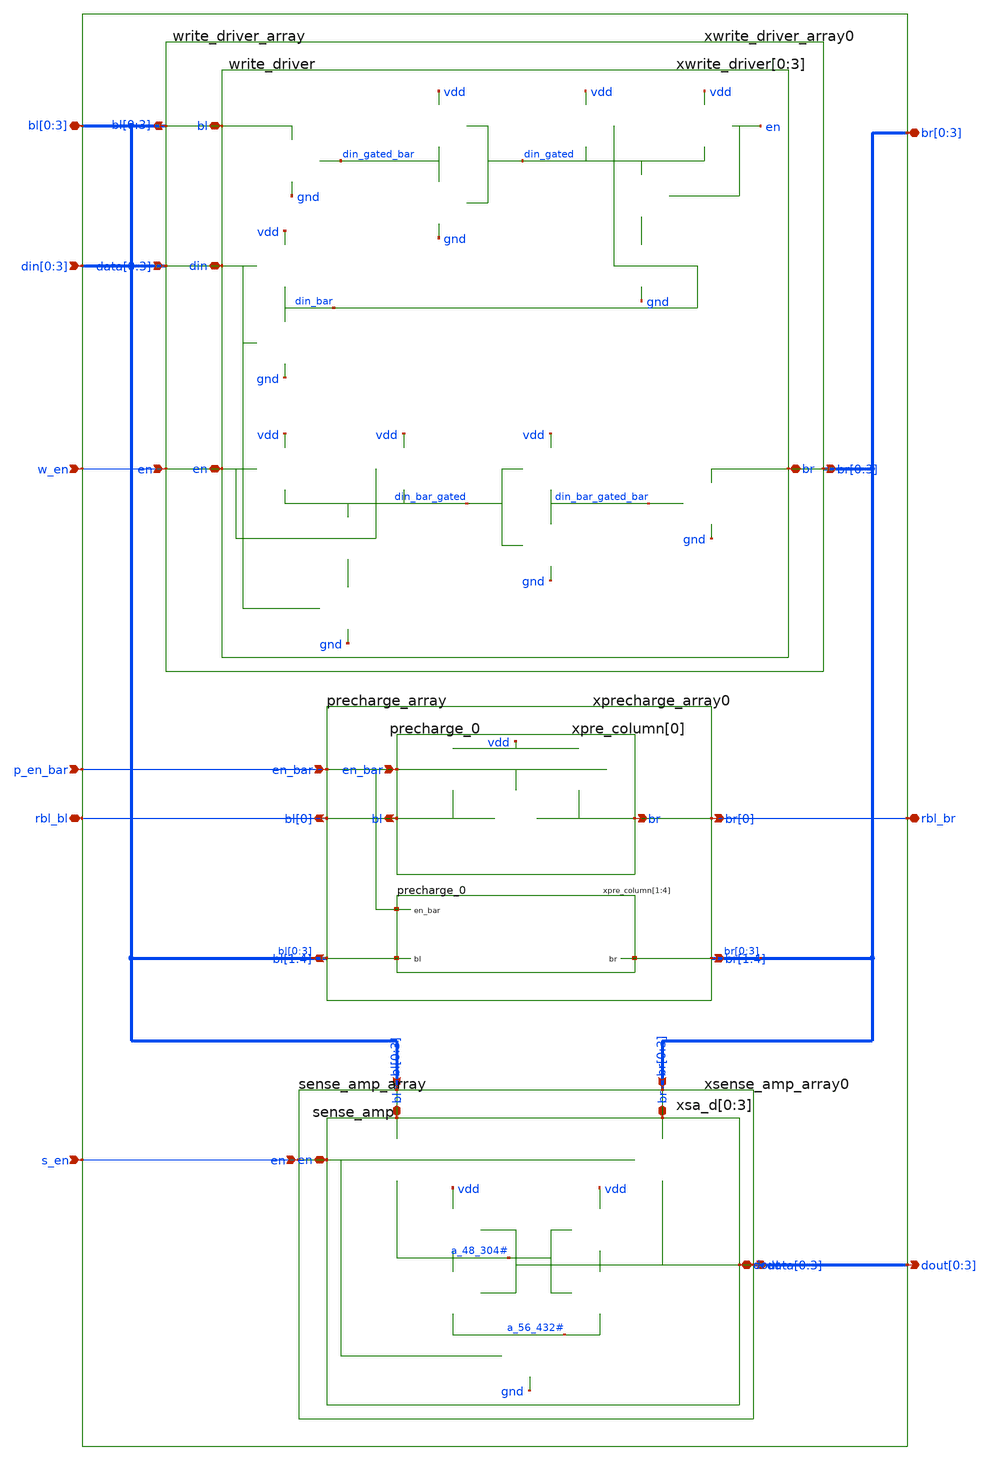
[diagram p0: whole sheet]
** sch_path: sram_4_16_scn4m/port_data.sch
**.subckt port_data rbl_bl rbl_br bl[0],bl[1],bl[2],bl[3] br[0],br[1],br[2],br[3]
*+ dout[0],dout[1],dout[2],dout[3] din[0],din[1],din[2],din[3] s_en p_en_bar w_en
*.iopin rbl_bl
*.iopin rbl_br
*.iopin bl[0],bl[1],bl[2],bl[3]
*.iopin br[0],br[1],br[2],br[3]
*.opin dout[0],dout[1],dout[2],dout[3]
*.ipin din[0],din[1],din[2],din[3]
*.ipin s_en
*.ipin p_en_bar
*.ipin w_en
xprecharge_array0 p_en_bar vdd precharge_array
xwrite_driver_array0 din[0] din[1] din[2] din[3] bl[0] bl[1] bl[2] bl[3] br[0] br[1] br[2] br[3]
+ w_en vdd gnd write_driver_array
xsense_amp_array0 dout[0] dout[1] dout[2] dout[3] bl[0] bl[1] bl[2] bl[3] br[0] br[1] br[2] br[3]
+ s_en vdd gnd sense_amp_array
**.ends

* expanding   symbol:  precharge_array.sch # of pins=5
** sym_path: sram_4_16_scn4m/precharge_array.sch
** sch_path: sram_4_16_scn4m/precharge_array.sch
.subckt precharge_array en_bar vdd
*.opin bl[0]
*.opin br[0]
*.ipin en_bar
*.opin bl[1],bl[2],bl[3],bl[4]
*.opin br[1],br[2],br[3],br[4]
xpre_column[0] bl[0] br[0] en_bar vdd precharge_0
xpre_column[1] bl[1] br[1] en_bar vdd precharge_0
xpre_column[2] bl[2] br[2] en_bar vdd precharge_0
xpre_column[3] bl[3] br[3] en_bar vdd precharge_0
xpre_column[4] bl[4] br[4] en_bar vdd precharge_0
.ends


* expanding   symbol:  write_driver_array.sch # of pins=4
** sym_path: sram_4_16_scn4m/write_driver_array.sch
** sch_path: sram_4_16_scn4m/write_driver_array.sch
.subckt write_driver_array data[0] data[1] data[2] data[3] bl[0] bl[1] bl[2] bl[3] br[0] br[1] br[2]
+ br[3] en vdd gnd
*.ipin data[0],data[1],data[2],data[3]
*.opin bl[0],bl[1],bl[2],bl[3]
*.opin br[0],br[1],br[2],br[3]
*.ipin en
xwrite_driver[0] data[0] bl[0] br[0] en vdd gnd write_driver
xwrite_driver[1] data[1] bl[1] br[1] en vdd gnd write_driver
xwrite_driver[2] data[2] bl[2] br[2] en vdd gnd write_driver
xwrite_driver[3] data[3] bl[3] br[3] en vdd gnd write_driver
.ends


* expanding   symbol:  sense_amp_array.sch # of pins=4
** sym_path: sram_4_16_scn4m/sense_amp_array.sch
** sch_path: sram_4_16_scn4m/sense_amp_array.sch
.subckt sense_amp_array data[0] data[1] data[2] data[3] bl[0] bl[1] bl[2] bl[3] br[0] br[1] br[2]
+ br[3] en vdd gnd
*.opin data[0],data[1],data[2],data[3]
*.ipin bl[0],bl[1],bl[2],bl[3]
*.ipin br[0],br[1],br[2],br[3]
*.ipin en
xsa_d[0] bl[0] br[0] data[0] en vdd gnd sense_amp
xsa_d[1] bl[1] br[1] data[1] en vdd gnd sense_amp
xsa_d[2] bl[2] br[2] data[2] en vdd gnd sense_amp
xsa_d[3] bl[3] br[3] data[3] en vdd gnd sense_amp
.ends


* expanding   symbol:  precharge_0.sch # of pins=3
** sym_path: sram_4_16_scn4m/precharge_0.sch
** sch_path: sram_4_16_scn4m/precharge_0.sch
.subckt precharge_0 bl br en_bar vdd
*.opin bl
*.opin br
*.ipin en_bar
XMupper_pmos1 bl en_bar vdd vdd sky130_fd_pr__pfet_01v8 L=0.4 W=1.6 nf=1 ad='int((nf+1)/2) * W/nf * 0.29'
+ as='int((nf+2)/2) * W/nf * 0.29' pd='2*int((nf+1)/2) * (W/nf + 0.29)' ps='2*int((nf+2)/2) * (W/nf + 0.29)'
+ nrd='0.29 / W' nrs='0.29 / W' sa=0 sb=0 sd=0 mult=1 m=1
XMupper_pmos2 br en_bar vdd vdd sky130_fd_pr__pfet_01v8 L=0.4 W=1.6 nf=1 ad='int((nf+1)/2) * W/nf * 0.29'
+ as='int((nf+2)/2) * W/nf * 0.29' pd='2*int((nf+1)/2) * (W/nf + 0.29)' ps='2*int((nf+2)/2) * (W/nf + 0.29)'
+ nrd='0.29 / W' nrs='0.29 / W' sa=0 sb=0 sd=0 mult=1 m=1
XMlower_pmos br en_bar bl vdd sky130_fd_pr__pfet_01v8 L=0.4 W=1.6 nf=1 ad='int((nf+1)/2) * W/nf * 0.29'
+ as='int((nf+2)/2) * W/nf * 0.29' pd='2*int((nf+1)/2) * (W/nf + 0.29)' ps='2*int((nf+2)/2) * (W/nf + 0.29)'
+ nrd='0.29 / W' nrs='0.29 / W' sa=0 sb=0 sd=0 mult=1 m=1
.ends


* expanding   symbol:  write_driver.sch # of pins=4
** sym_path: sram_4_16_scn4m/write_driver.sch
** sch_path: sram_4_16_scn4m/write_driver.sch
.subckt write_driver din bl br en vdd gnd
*.iopin din
*.iopin bl
*.iopin br
*.iopin en
XM_1 din_bar din gnd gnd sky130_fd_pr__nfet_01v8 L=0.4 W=1.4 nf=1 ad='int((nf+1)/2) * W/nf * 0.29' as='int((nf+2)/2) * W/nf * 0.29'
+ pd='2*int((nf+1)/2) * (W/nf + 0.29)' ps='2*int((nf+2)/2) * (W/nf + 0.29)' nrd='0.29 / W' nrs='0.29 / W'
+ sa=0 sb=0 sd=0 mult=1 m=1
XM_2 din_bar din vdd vdd sky130_fd_pr__pfet_01v8 L=0.4 W=1.4 nf=1 ad='int((nf+1)/2) * W/nf * 0.29' as='int((nf+2)/2) * W/nf * 0.29'
+ pd='2*int((nf+1)/2) * (W/nf + 0.29)' ps='2*int((nf+2)/2) * (W/nf + 0.29)' nrd='0.29 / W' nrs='0.29 / W'
+ sa=0 sb=0 sd=0 mult=1 m=1
XM_6 din_bar_gated en vdd vdd sky130_fd_pr__pfet_01v8 L=0.4 W=1.4 nf=1 ad='int((nf+1)/2) * W/nf * 0.29'
+ as='int((nf+2)/2) * W/nf * 0.29' pd='2*int((nf+1)/2) * (W/nf + 0.29)' ps='2*int((nf+2)/2) * (W/nf + 0.29)'
+ nrd='0.29 / W' nrs='0.29 / W' sa=0 sb=0 sd=0 mult=1 m=1
XM_5 din_bar_gated en vdd vdd sky130_fd_pr__pfet_01v8 L=0.4 W=1.4 nf=1 ad='int((nf+1)/2) * W/nf * 0.29'
+ as='int((nf+2)/2) * W/nf * 0.29' pd='2*int((nf+1)/2) * (W/nf + 0.29)' ps='2*int((nf+2)/2) * (W/nf + 0.29)'
+ nrd='0.29 / W' nrs='0.29 / W' sa=0 sb=0 sd=0 mult=1 m=1
XM_3 din_bar_gated en net1 gnd sky130_fd_pr__nfet_01v8 L=0.4 W=1.4 nf=1 ad='int((nf+1)/2) * W/nf * 0.29'
+ as='int((nf+2)/2) * W/nf * 0.29' pd='2*int((nf+1)/2) * (W/nf + 0.29)' ps='2*int((nf+2)/2) * (W/nf + 0.29)'
+ nrd='0.29 / W' nrs='0.29 / W' sa=0 sb=0 sd=0 mult=1 m=1
XM_4 net1 din gnd gnd sky130_fd_pr__nfet_01v8 L=0.4 W=1.4 nf=1 ad='int((nf+1)/2) * W/nf * 0.29' as='int((nf+2)/2) * W/nf * 0.29'
+ pd='2*int((nf+1)/2) * (W/nf + 0.29)' ps='2*int((nf+2)/2) * (W/nf + 0.29)' nrd='0.29 / W' nrs='0.29 / W'
+ sa=0 sb=0 sd=0 mult=1 m=1
XM_7 din_bar_gated_bar din_bar_gated gnd gnd sky130_fd_pr__nfet_01v8 L=0.4 W=1.4 nf=1 ad='int((nf+1)/2) * W/nf * 0.29'
+ as='int((nf+2)/2) * W/nf * 0.29' pd='2*int((nf+1)/2) * (W/nf + 0.29)' ps='2*int((nf+2)/2) * (W/nf + 0.29)'
+ nrd='0.29 / W' nrs='0.29 / W' sa=0 sb=0 sd=0 mult=1 m=1
XM_8 din_bar_gated_bar din_bar_gated vdd vdd sky130_fd_pr__pfet_01v8 L=0.4 W=1.4 nf=1 ad='int((nf+1)/2) * W/nf * 0.29'
+ as='int((nf+2)/2) * W/nf * 0.29' pd='2*int((nf+1)/2) * (W/nf + 0.29)' ps='2*int((nf+2)/2) * (W/nf + 0.29)'
+ nrd='0.29 / W' nrs='0.29 / W' sa=0 sb=0 sd=0 mult=1 m=1
XM_9 din_gated en vdd vdd sky130_fd_pr__pfet_01v8 L=0.4 W=1.4 nf=1 ad='int((nf+1)/2) * W/nf * 0.29' as='int((nf+2)/2) * W/nf * 0.29'
+ pd='2*int((nf+1)/2) * (W/nf + 0.29)' ps='2*int((nf+2)/2) * (W/nf + 0.29)' nrd='0.29 / W' nrs='0.29 / W'
+ sa=0 sb=0 sd=0 mult=1 m=1
XM_12 din_gated din_bar vdd vdd sky130_fd_pr__pfet_01v8 L=0.4 W=1.4 nf=1 ad='int((nf+1)/2) * W/nf * 0.29'
+ as='int((nf+2)/2) * W/nf * 0.29' pd='2*int((nf+1)/2) * (W/nf + 0.29)' ps='2*int((nf+2)/2) * (W/nf + 0.29)'
+ nrd='0.29 / W' nrs='0.29 / W' sa=0 sb=0 sd=0 mult=1 m=1
XM_10 din_gated en net2 gnd sky130_fd_pr__nfet_01v8 L=0.4 W=1.4 nf=1 ad='int((nf+1)/2) * W/nf * 0.29'
+ as='int((nf+2)/2) * W/nf * 0.29' pd='2*int((nf+1)/2) * (W/nf + 0.29)' ps='2*int((nf+2)/2) * (W/nf + 0.29)'
+ nrd='0.29 / W' nrs='0.29 / W' sa=0 sb=0 sd=0 mult=1 m=1
XM_11 net2 din_bar gnd gnd sky130_fd_pr__nfet_01v8 L=0.4 W=1.4 nf=1 ad='int((nf+1)/2) * W/nf * 0.29'
+ as='int((nf+2)/2) * W/nf * 0.29' pd='2*int((nf+1)/2) * (W/nf + 0.29)' ps='2*int((nf+2)/2) * (W/nf + 0.29)'
+ nrd='0.29 / W' nrs='0.29 / W' sa=0 sb=0 sd=0 mult=1 m=1
XM_14 din_gated_bar din_gated gnd gnd sky130_fd_pr__nfet_01v8 L=0.4 W=1.4 nf=1 ad='int((nf+1)/2) * W/nf * 0.29'
+ as='int((nf+2)/2) * W/nf * 0.29' pd='2*int((nf+1)/2) * (W/nf + 0.29)' ps='2*int((nf+2)/2) * (W/nf + 0.29)'
+ nrd='0.29 / W' nrs='0.29 / W' sa=0 sb=0 sd=0 mult=1 m=1
XM_13 din_gated_bar din_gated vdd vdd sky130_fd_pr__pfet_01v8 L=0.4 W=1.4 nf=1 ad='int((nf+1)/2) * W/nf * 0.29'
+ as='int((nf+2)/2) * W/nf * 0.29' pd='2*int((nf+1)/2) * (W/nf + 0.29)' ps='2*int((nf+2)/2) * (W/nf + 0.29)'
+ nrd='0.29 / W' nrs='0.29 / W' sa=0 sb=0 sd=0 mult=1 m=1
XM_15 bl din_gated_bar gnd gnd sky130_fd_pr__nfet_01v8 L=0.4 W=2.4 nf=1 ad='int((nf+1)/2) * W/nf * 0.29'
+ as='int((nf+2)/2) * W/nf * 0.29' pd='2*int((nf+1)/2) * (W/nf + 0.29)' ps='2*int((nf+2)/2) * (W/nf + 0.29)'
+ nrd='0.29 / W' nrs='0.29 / W' sa=0 sb=0 sd=0 mult=1 m=1
XM_16 br din_bar_gated_bar gnd gnd sky130_fd_pr__nfet_01v8 L=0.4 W=2.4 nf=1 ad='int((nf+1)/2) * W/nf * 0.29'
+ as='int((nf+2)/2) * W/nf * 0.29' pd='2*int((nf+1)/2) * (W/nf + 0.29)' ps='2*int((nf+2)/2) * (W/nf + 0.29)'
+ nrd='0.29 / W' nrs='0.29 / W' sa=0 sb=0 sd=0 mult=1 m=1
.ends


* expanding   symbol:  sense_amp.sch # of pins=4
** sym_path: sram_4_16_scn4m/sense_amp.sch
** sch_path: sram_4_16_scn4m/sense_amp.sch
.subckt sense_amp bl br dout en vdd gnd
*.iopin bl
*.iopin br
*.iopin dout
*.iopin en
XM1004 a_48_304# dout vdd vdd sky130_fd_pr__pfet_01v8 L=0.15 W=1 nf=1 ad='int((nf+1)/2) * W/nf * 0.29'
+ as='int((nf+2)/2) * W/nf * 0.29' pd='2*int((nf+1)/2) * (W/nf + 0.29)' ps='2*int((nf+2)/2) * (W/nf + 0.29)'
+ nrd='0.29 / W' nrs='0.29 / W' sa=0 sb=0 sd=0 mult=1 m=1
XM1003 dout a_48_304# vdd vdd sky130_fd_pr__pfet_01v8 L=0.4 W=3.6 nf=1 ad='int((nf+1)/2) * W/nf * 0.29'
+ as='int((nf+2)/2) * W/nf * 0.29' pd='2*int((nf+1)/2) * (W/nf + 0.29)' ps='2*int((nf+2)/2) * (W/nf + 0.29)'
+ nrd='0.29 / W' nrs='0.29 / W' sa=0 sb=0 sd=0 mult=1 m=1
XM1002 a_48_304# dout a_56_432# gnd sky130_fd_pr__nfet_01v8 L=0.4 W=1.8 nf=1 ad='int((nf+1)/2) * W/nf * 0.29'
+ as='int((nf+2)/2) * W/nf * 0.29' pd='2*int((nf+1)/2) * (W/nf + 0.29)' ps='2*int((nf+2)/2) * (W/nf + 0.29)'
+ nrd='0.29 / W' nrs='0.29 / W' sa=0 sb=0 sd=0 mult=1 m=1
XM1001 dout a_48_304# a_56_432# gnd sky130_fd_pr__nfet_01v8 L=0.4 W=1.8 nf=1 ad='int((nf+1)/2) * W/nf * 0.29'
+ as='int((nf+2)/2) * W/nf * 0.29' pd='2*int((nf+1)/2) * (W/nf + 0.29)' ps='2*int((nf+2)/2) * (W/nf + 0.29)'
+ nrd='0.29 / W' nrs='0.29 / W' sa=0 sb=0 sd=0 mult=1 m=1
XM1000 a_56_432# en gnd gnd sky130_fd_pr__nfet_01v8 L=0.4 W=1.8 nf=1 ad='int((nf+1)/2) * W/nf * 0.29'
+ as='int((nf+2)/2) * W/nf * 0.29' pd='2*int((nf+1)/2) * (W/nf + 0.29)' ps='2*int((nf+2)/2) * (W/nf + 0.29)'
+ nrd='0.29 / W' nrs='0.29 / W' sa=0 sb=0 sd=0 mult=1 m=1
XM1006 a_48_304# en bl vdd sky130_fd_pr__pfet_01v8 L=0.4 W=4.8 nf=1 ad='int((nf+1)/2) * W/nf * 0.29'
+ as='int((nf+2)/2) * W/nf * 0.29' pd='2*int((nf+1)/2) * (W/nf + 0.29)' ps='2*int((nf+2)/2) * (W/nf + 0.29)'
+ nrd='0.29 / W' nrs='0.29 / W' sa=0 sb=0 sd=0 mult=1 m=1
XM1005 dout en br vdd sky130_fd_pr__pfet_01v8 L=0.4 W=4.8 nf=1 ad='int((nf+1)/2) * W/nf * 0.29' as='int((nf+2)/2) * W/nf * 0.29'
+ pd='2*int((nf+1)/2) * (W/nf + 0.29)' ps='2*int((nf+2)/2) * (W/nf + 0.29)' nrd='0.29 / W' nrs='0.29 / W'
+ sa=0 sb=0 sd=0 mult=1 m=1
.ends

.end
